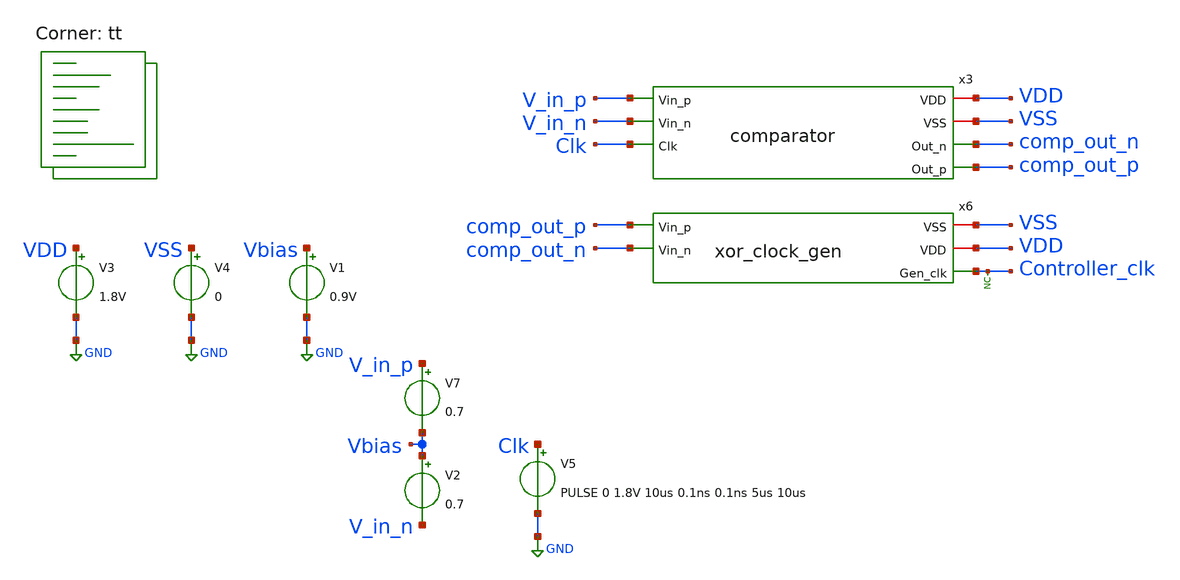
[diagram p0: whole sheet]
** sch_path: xschem/tests/sar_adc/xor_comparator.sch
**.subckt xor_comparator
V3 VDD GND 1.8V
V4 VSS GND 0
V2 Vbias V_in_n 0.7
V5 Clk GND PULSE 0 1.8V 10us 0.1ns 0.1ns 5us 10us
V1 Vbias GND 0.9V
V7 V_in_p Vbias 0.7
x3 VDD VSS V_in_p comp_out_n V_in_n comp_out_p Clk comparator
x6 VSS comp_out_p VDD comp_out_n Controller_clk xor_clock_gen
* noconn Controller_clk
**** begin user architecture code
 * .lib $::SKYWATER_MODELS/sky130.lib.spice tt
.include $::SKYWATER_STDCELLS/sky130_fd_sc_hd.spice


.options acct list
.temp 25
*vvcc VDD 0 dc 1.8
*vvss VSS 0 0
.control
tran 0.1u 60u
*plot RST_PLS clk+2 Pulse+4
*plot Done-4 V_in_p-V_in_n-2 bits1 bits2+2 bits3+4 bits4+6 bits5+8 bits6+10 bits7+12 bits8+14
*+ bits9+16 bits10+18
* plot x1.vsampled_p x1.vsampled_n x1.vsampled_p-x1.vsampled_n x1.sw_sample-2 x1.comp_out_p+2
plot comp_out_n comp_out_p+2 controller_clk+4
write xor_comparator.raw
.endc


.lib $::SKYWATER_MODELS/sky130.lib.spice tt
**** end user architecture code
**.ends

* expanding   symbol:  src/comparator/comparator.sym # of pins=7
** sym_path: xschem/src/comparator/comparator.sym
** sch_path: xschem/src/comparator/comparator.sch
.subckt comparator VDD VSS Vin_p Out_n Vin_n Out_p Clk
*.iopin VDD
*.iopin VSS
*.ipin Vin_p
*.opin Out_n
*.ipin Vin_n
*.opin Out_p
*.ipin Clk
XM1 Pre_Amp_n Clk VDD VSS sky130_fd_pr__pfet_01v8 L=0.15 W=1 nf=1 ad='int((nf+1)/2) * W/nf * 0.29' as='int((nf+2)/2) * W/nf * 0.29'
+ pd='2*int((nf+1)/2) * (W/nf + 0.29)' ps='2*int((nf+2)/2) * (W/nf + 0.29)' nrd='0.29 / W' nrs='0.29 / W'
+ sa=0 sb=0 sd=0 mult=1 m=1
XM2 Pre_Amp_p Clk VDD VSS sky130_fd_pr__pfet_01v8 L=0.15 W=1 nf=1 ad='int((nf+1)/2) * W/nf * 0.29' as='int((nf+2)/2) * W/nf * 0.29'
+ pd='2*int((nf+1)/2) * (W/nf + 0.29)' ps='2*int((nf+2)/2) * (W/nf + 0.29)' nrd='0.29 / W' nrs='0.29 / W'
+ sa=0 sb=0 sd=0 mult=1 m=1
XM3 Pre_Amp_p Vin_p net1 VSS sky130_fd_pr__nfet_01v8 L=0.15 W=1 nf=1 ad='int((nf+1)/2) * W/nf * 0.29'
+ as='int((nf+2)/2) * W/nf * 0.29' pd='2*int((nf+1)/2) * (W/nf + 0.29)' ps='2*int((nf+2)/2) * (W/nf + 0.29)'
+ nrd='0.29 / W' nrs='0.29 / W' sa=0 sb=0 sd=0 mult=1 m=1
XM4 Pre_Amp_n Vin_n net1 VSS sky130_fd_pr__nfet_01v8 L=0.15 W=1 nf=1 ad='int((nf+1)/2) * W/nf * 0.29'
+ as='int((nf+2)/2) * W/nf * 0.29' pd='2*int((nf+1)/2) * (W/nf + 0.29)' ps='2*int((nf+2)/2) * (W/nf + 0.29)'
+ nrd='0.29 / W' nrs='0.29 / W' sa=0 sb=0 sd=0 mult=1 m=1
XM5 net3 Out_p VDD VSS sky130_fd_pr__pfet_01v8 L=0.15 W=1 nf=1 ad='int((nf+1)/2) * W/nf * 0.29' as='int((nf+2)/2) * W/nf * 0.29'
+ pd='2*int((nf+1)/2) * (W/nf + 0.29)' ps='2*int((nf+2)/2) * (W/nf + 0.29)' nrd='0.29 / W' nrs='0.29 / W'
+ sa=0 sb=0 sd=0 mult=1 m=1
XM6 net2 Out_n VDD VSS sky130_fd_pr__pfet_01v8 L=0.15 W=1 nf=1 ad='int((nf+1)/2) * W/nf * 0.29' as='int((nf+2)/2) * W/nf * 0.29'
+ pd='2*int((nf+1)/2) * (W/nf + 0.29)' ps='2*int((nf+2)/2) * (W/nf + 0.29)' nrd='0.29 / W' nrs='0.29 / W'
+ sa=0 sb=0 sd=0 mult=1 m=1
XM7 net2 Pre_Amp_p Out_p VSS sky130_fd_pr__nfet_01v8 L=0.15 W=1 nf=1 ad='int((nf+1)/2) * W/nf * 0.29'
+ as='int((nf+2)/2) * W/nf * 0.29' pd='2*int((nf+1)/2) * (W/nf + 0.29)' ps='2*int((nf+2)/2) * (W/nf + 0.29)'
+ nrd='0.29 / W' nrs='0.29 / W' sa=0 sb=0 sd=0 mult=1 m=1
XM8 net3 Pre_Amp_n Out_n VSS sky130_fd_pr__nfet_01v8 L=0.15 W=1 nf=1 ad='int((nf+1)/2) * W/nf * 0.29'
+ as='int((nf+2)/2) * W/nf * 0.29' pd='2*int((nf+1)/2) * (W/nf + 0.29)' ps='2*int((nf+2)/2) * (W/nf + 0.29)'
+ nrd='0.29 / W' nrs='0.29 / W' sa=0 sb=0 sd=0 mult=1 m=1
XM9 net1 Clk VSS VSS sky130_fd_pr__nfet_01v8 L=0.15 W=1 nf=1 ad='int((nf+1)/2) * W/nf * 0.29' as='int((nf+2)/2) * W/nf * 0.29'
+ pd='2*int((nf+1)/2) * (W/nf + 0.29)' ps='2*int((nf+2)/2) * (W/nf + 0.29)' nrd='0.29 / W' nrs='0.29 / W'
+ sa=0 sb=0 sd=0 mult=1 m=1
XM10 Pre_Amp_n Vin_n net1 VSS sky130_fd_pr__nfet_01v8 L=0.15 W=1 nf=1 ad='int((nf+1)/2) * W/nf * 0.29'
+ as='int((nf+2)/2) * W/nf * 0.29' pd='2*int((nf+1)/2) * (W/nf + 0.29)' ps='2*int((nf+2)/2) * (W/nf + 0.29)'
+ nrd='0.29 / W' nrs='0.29 / W' sa=0 sb=0 sd=0 mult=1 m=1
XM11 Out_n Clk_n VSS VSS sky130_fd_pr__nfet_01v8 L=0.15 W=1 nf=1 ad='int((nf+1)/2) * W/nf * 0.29' as='int((nf+2)/2) * W/nf * 0.29'
+ pd='2*int((nf+1)/2) * (W/nf + 0.29)' ps='2*int((nf+2)/2) * (W/nf + 0.29)' nrd='0.29 / W' nrs='0.29 / W'
+ sa=0 sb=0 sd=0 mult=1 m=1
XM12 Out_n Out_p VSS VSS sky130_fd_pr__nfet_01v8 L=0.15 W=1 nf=1 ad='int((nf+1)/2) * W/nf * 0.29' as='int((nf+2)/2) * W/nf * 0.29'
+ pd='2*int((nf+1)/2) * (W/nf + 0.29)' ps='2*int((nf+2)/2) * (W/nf + 0.29)' nrd='0.29 / W' nrs='0.29 / W'
+ sa=0 sb=0 sd=0 mult=1 m=1
XM13 Out_p Out_n VSS VSS sky130_fd_pr__nfet_01v8 L=0.15 W=1 nf=1 ad='int((nf+1)/2) * W/nf * 0.29' as='int((nf+2)/2) * W/nf * 0.29'
+ pd='2*int((nf+1)/2) * (W/nf + 0.29)' ps='2*int((nf+2)/2) * (W/nf + 0.29)' nrd='0.29 / W' nrs='0.29 / W'
+ sa=0 sb=0 sd=0 mult=1 m=1
XM14 Out_p Clk_n VSS VSS sky130_fd_pr__nfet_01v8 L=0.15 W=1 nf=1 ad='int((nf+1)/2) * W/nf * 0.29' as='int((nf+2)/2) * W/nf * 0.29'
+ pd='2*int((nf+1)/2) * (W/nf + 0.29)' ps='2*int((nf+2)/2) * (W/nf + 0.29)' nrd='0.29 / W' nrs='0.29 / W'
+ sa=0 sb=0 sd=0 mult=1 m=1
XM15 Clk_n Clk VDD VSS sky130_fd_pr__pfet_01v8 L=0.15 W=1 nf=1 ad='int((nf+1)/2) * W/nf * 0.29' as='int((nf+2)/2) * W/nf * 0.29'
+ pd='2*int((nf+1)/2) * (W/nf + 0.29)' ps='2*int((nf+2)/2) * (W/nf + 0.29)' nrd='0.29 / W' nrs='0.29 / W'
+ sa=0 sb=0 sd=0 mult=1 m=1
XM16 Clk_n Clk VSS VSS sky130_fd_pr__nfet_01v8 L=0.15 W=1 nf=1 ad='int((nf+1)/2) * W/nf * 0.29' as='int((nf+2)/2) * W/nf * 0.29'
+ pd='2*int((nf+1)/2) * (W/nf + 0.29)' ps='2*int((nf+2)/2) * (W/nf + 0.29)' nrd='0.29 / W' nrs='0.29 / W'
+ sa=0 sb=0 sd=0 mult=1 m=1
.ends


* expanding   symbol:  src/xor_clock_gen/xor_clock_gen.sym # of pins=5
** sym_path: xschem/src/xor_clock_gen/xor_clock_gen.sym
** sch_path: xschem/src/xor_clock_gen/xor_clock_gen.sch
.subckt xor_clock_gen VSS Vin_p VDD Vin_n Gen_clk
*.ipin Vin_p
*.iopin VSS
*.opin Gen_clk
*.iopin VDD
*.ipin Vin_n
x2 Vin_p Vin_n VSS VSS VDD VDD net1 sky130_fd_sc_hd__xor2_1
x3 net1 VSS VSS VDD VDD net2 sky130_fd_sc_hd__clkdlybuf4s50_1
x17 net2 VSS VSS VDD VDD net3 sky130_fd_sc_hd__clkdlybuf4s50_1
x9 net14 VSS VSS VDD VDD net4 sky130_fd_sc_hd__clkbuf_1
x14 net4 VSS VSS VDD VDD net5 sky130_fd_sc_hd__clkbuf_2
x19 net5 VSS VSS VDD VDD net6 sky130_fd_sc_hd__clkbuf_4
x26 net6 VSS VSS VDD VDD net7 sky130_fd_sc_hd__clkbuf_8
x27 net7 VSS VSS VDD VDD Gen_clk sky130_fd_sc_hd__clkbuf_16
XC1 net7 VSS sky130_fd_pr__cap_mim_m3_1 W=3 L=3 MF=3 m=3
x1 net3 VSS VSS VDD VDD net9 sky130_fd_sc_hd__clkdlybuf4s50_1
x4 net9 VSS VSS VDD VDD net8 sky130_fd_sc_hd__clkdlybuf4s50_1
x5 net8 VSS VSS VDD VDD net10 sky130_fd_sc_hd__clkdlybuf4s50_1
x7 net11 VSS VSS VDD VDD net15 sky130_fd_sc_hd__clkdlybuf4s50_1
x8 net15 VSS VSS VDD VDD net16 sky130_fd_sc_hd__clkdlybuf4s50_1
x10 net16 VSS VSS VDD VDD net17 sky130_fd_sc_hd__clkdlybuf4s50_1
x11 net17 VSS VSS VDD VDD net19 sky130_fd_sc_hd__clkdlybuf4s50_1
x12 net20 VSS VSS VDD VDD net21 sky130_fd_sc_hd__clkdlybuf4s50_1
x13 net21 VSS VSS VDD VDD net12 sky130_fd_sc_hd__clkdlybuf4s50_1
x15 net12 VSS VSS VDD VDD net13 sky130_fd_sc_hd__clkdlybuf4s50_1
x16 net13 VSS VSS VDD VDD net22 sky130_fd_sc_hd__clkdlybuf4s50_1
x18 net22 VSS VSS VDD VDD net14 sky130_fd_sc_hd__clkdlybuf4s50_1
x6 net10 VSS VSS VDD VDD net11 sky130_fd_sc_hd__clkdlybuf4s50_1
x20 net19 VSS VSS VDD VDD net18 sky130_fd_sc_hd__clkdlybuf4s50_1
x21 net18 VSS VSS VDD VDD net20 sky130_fd_sc_hd__clkdlybuf4s50_1
.ends

.GLOBAL GND
.end
